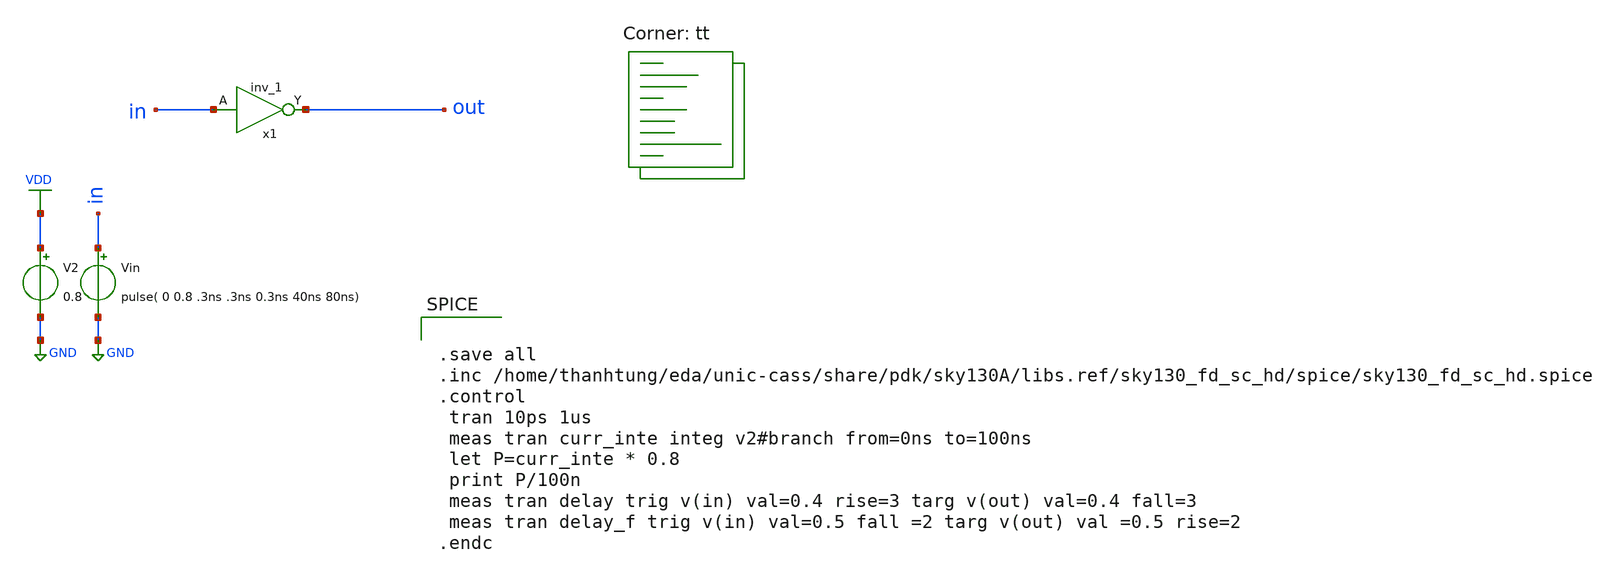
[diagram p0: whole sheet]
** sch_path: d_inver_para.sch
**.subckt d_inver_para
x1 in GND GND VDD VDD out sky130_fd_sc_hd__inv_1
V2 VDD GND 0.8
Vin in GND pulse( 0 0.8 .3ns .3ns 0.3ns 40ns 80ns)
**** begin user architecture code
.lib $::SKYWATER_MODELS/sky130.lib.spice tt


.save all
.inc /home/thanhtung/eda/unic-cass/share/pdk/sky130A/libs.ref/sky130_fd_sc_hd/spice/sky130_fd_sc_hd.spice
.control
 tran 10ps 1us
 meas tran curr_inte integ v2#branch from=0ns to=100ns
 let P=curr_inte * 0.8
 print P/100n
 meas tran delay trig v(in) val=0.4 rise=3 targ v(out) val=0.4 fall=3
 meas tran delay_f trig v(in) val=0.5 fall =2 targ v(out) val =0.5 rise=2
.endc


**** end user architecture code
**.ends
.GLOBAL GND
.GLOBAL VDD
.end
